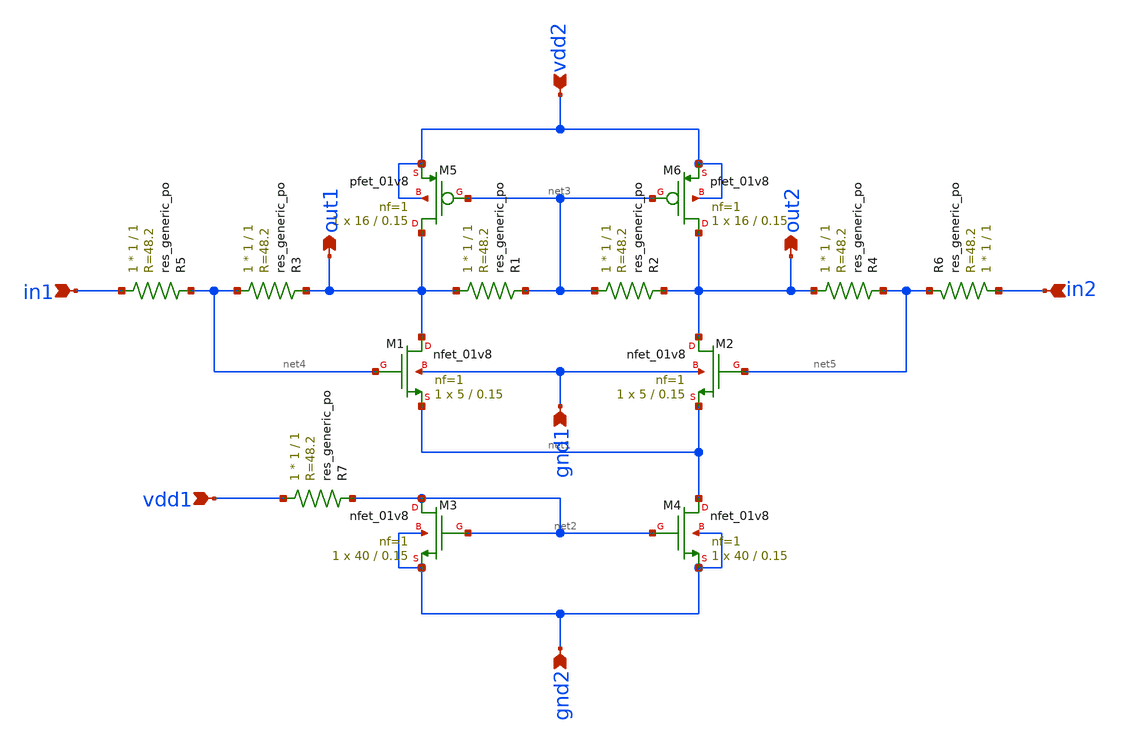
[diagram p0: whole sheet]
** sch_path: xschem/lownoiseamplifier/cmfb-negfb-revision.sch
**.subckt cmfb-negfb-revision gnd1 gnd2 vdd1 vdd2 in1 in2 out1 out2
*.ipin gnd1
*.ipin gnd2
*.ipin vdd1
*.ipin vdd2
*.ipin in1
*.ipin in2
*.opin out1
*.opin out2
XM1 out1 net4 net1 gnd1 sky130_fd_pr__nfet_01v8 L=0.15 W=5 nf=1 ad='int((nf+1)/2) * W/nf * 0.29' as='int((nf+2)/2) * W/nf * 0.29'
+ pd='2*int((nf+1)/2) * (W/nf + 0.29)' ps='2*int((nf+2)/2) * (W/nf + 0.29)' nrd='0.29 / W' nrs='0.29 / W'
+ sa=0 sb=0 sd=0 mult=1 m=1
XM2 out2 net5 net1 gnd1 sky130_fd_pr__nfet_01v8 L=0.15 W=5 nf=1 ad='int((nf+1)/2) * W/nf * 0.29' as='int((nf+2)/2) * W/nf * 0.29'
+ pd='2*int((nf+1)/2) * (W/nf + 0.29)' ps='2*int((nf+2)/2) * (W/nf + 0.29)' nrd='0.29 / W' nrs='0.29 / W'
+ sa=0 sb=0 sd=0 mult=1 m=1
XM3 net2 net2 gnd2 gnd2 sky130_fd_pr__nfet_01v8 L=0.15 W=40 nf=1 ad='int((nf+1)/2) * W/nf * 0.29' as='int((nf+2)/2) * W/nf * 0.29'
+ pd='2*int((nf+1)/2) * (W/nf + 0.29)' ps='2*int((nf+2)/2) * (W/nf + 0.29)' nrd='0.29 / W' nrs='0.29 / W'
+ sa=0 sb=0 sd=0 mult=1 m=1
XM4 net1 net2 gnd2 gnd2 sky130_fd_pr__nfet_01v8 L=0.15 W=40 nf=1 ad='int((nf+1)/2) * W/nf * 0.29' as='int((nf+2)/2) * W/nf * 0.29'
+ pd='2*int((nf+1)/2) * (W/nf + 0.29)' ps='2*int((nf+2)/2) * (W/nf + 0.29)' nrd='0.29 / W' nrs='0.29 / W'
+ sa=0 sb=0 sd=0 mult=1 m=1
XM5 out1 net3 vdd2 vdd2 sky130_fd_pr__pfet_01v8 L=0.15 W=16 nf=1 ad='int((nf+1)/2) * W/nf * 0.29' as='int((nf+2)/2) * W/nf * 0.29'
+ pd='2*int((nf+1)/2) * (W/nf + 0.29)' ps='2*int((nf+2)/2) * (W/nf + 0.29)' nrd='0.29 / W' nrs='0.29 / W'
+ sa=0 sb=0 sd=0 mult=1 m=1
XM6 out2 net3 vdd2 vdd2 sky130_fd_pr__pfet_01v8 L=0.15 W=16 nf=1 ad='int((nf+1)/2) * W/nf * 0.29' as='int((nf+2)/2) * W/nf * 0.29'
+ pd='2*int((nf+1)/2) * (W/nf + 0.29)' ps='2*int((nf+2)/2) * (W/nf + 0.29)' nrd='0.29 / W' nrs='0.29 / W'
+ sa=0 sb=0 sd=0 mult=1 m=1
XR1 out1 net3 sky130_fd_pr__res_generic_po W=1 L=1 m=1
XR2 net3 out2 sky130_fd_pr__res_generic_po W=1 L=1 m=1
XR3 net4 out1 sky130_fd_pr__res_generic_po W=1 L=1 m=1
XR4 out2 net5 sky130_fd_pr__res_generic_po W=1 L=1 m=1
XR5 in1 net4 sky130_fd_pr__res_generic_po W=1 L=1 m=1
XR6 in2 net5 sky130_fd_pr__res_generic_po W=1 L=1 m=1
XR7 vdd1 net2 sky130_fd_pr__res_generic_po W=1 L=1 m=1
**** begin user architecture code
 ** manual skywater pdks install (with patches applied)
* .lib $::SKYWATER_MODELS/models/sky130.lib.spice tt

** opencircuitdesign pdks install
.lib $::SKYWATER_MODELS/sky130.lib.spice tt

.param mc_mm_switch=0
.param mc_pr_switch=0

**** end user architecture code
**.ends
.end
